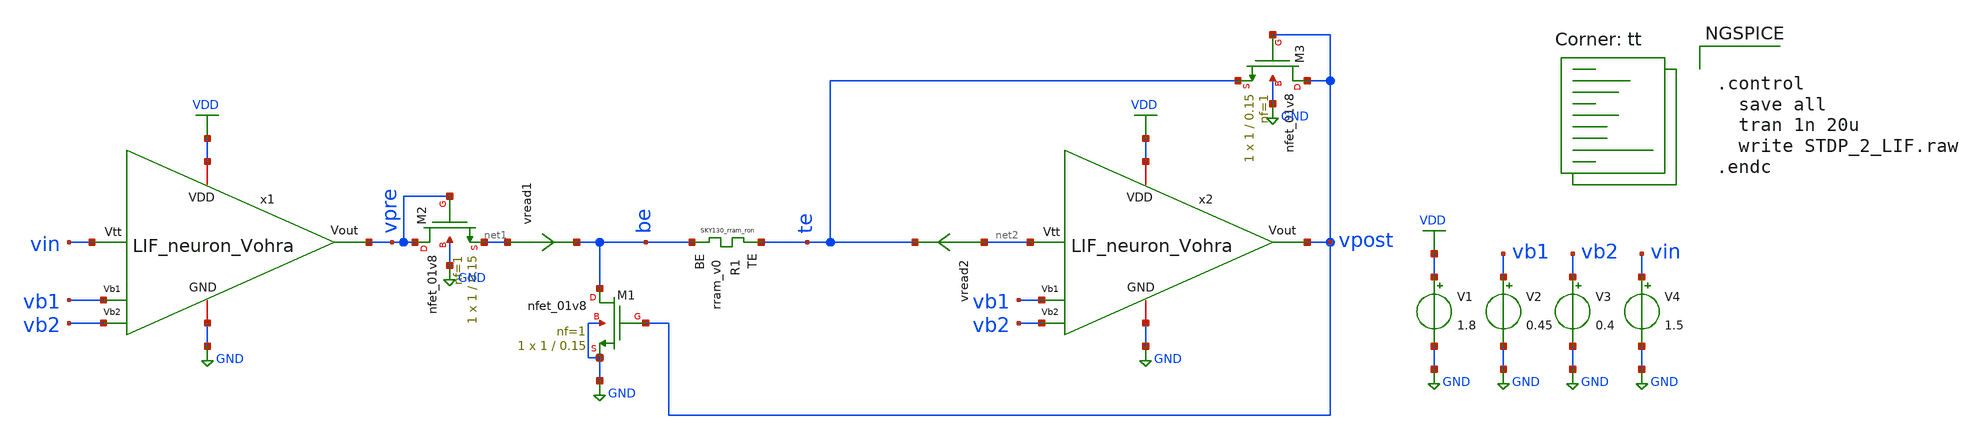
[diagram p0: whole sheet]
** sch_path: STDP/STDP_2_LIF.sch
**.subckt STDP_2_LIF
x1 VDD vpre vb1 vin GND vb2 LIF_neuron_Vohra
XR1 te be rram_v0
x2 VDD vpost vb1 net2 GND vb2 LIF_neuron_Vohra
vread1 net1 be 0
.save i(vread1)
XM1 be vpost GND GND sky130_fd_pr__nfet_01v8 L=0.15 W=1 nf=1 ad='int((nf+1)/2) * W/nf * 0.29' as='int((nf+2)/2) * W/nf * 0.29'
+ pd='2*int((nf+1)/2) * (W/nf + 0.29)' ps='2*int((nf+2)/2) * (W/nf + 0.29)' nrd='0.29 / W' nrs='0.29 / W'
+ sa=0 sb=0 sd=0 mult=1 m=1
V1 VDD GND 1.8
V4 vin GND 1.5
V2 vb1 GND 0.45
V3 vb2 GND 0.4
vread2 net2 te 0
.save i(vread2)
XM2 vpre vpre net1 GND sky130_fd_pr__nfet_01v8 L=0.15 W=1 nf=1 ad='int((nf+1)/2) * W/nf * 0.29' as='int((nf+2)/2) * W/nf * 0.29'
+ pd='2*int((nf+1)/2) * (W/nf + 0.29)' ps='2*int((nf+2)/2) * (W/nf + 0.29)' nrd='0.29 / W' nrs='0.29 / W'
+ sa=0 sb=0 sd=0 mult=1 m=1
XM3 vpost vpost te GND sky130_fd_pr__nfet_01v8 L=0.15 W=1 nf=1 ad='int((nf+1)/2) * W/nf * 0.29' as='int((nf+2)/2) * W/nf * 0.29'
+ pd='2*int((nf+1)/2) * (W/nf + 0.29)' ps='2*int((nf+2)/2) * (W/nf + 0.29)' nrd='0.29 / W' nrs='0.29 / W'
+ sa=0 sb=0 sd=0 mult=1 m=1
**** begin user architecture code
.lib $::SKYWATER_MODELS/sky130.lib.spice tt

** opencircuitdesign pdks install
.inc $::SKYWATER_MODELS/rram_v0.spice



.control
  save all
  tran 1n 20u
  write STDP_2_LIF.raw
.endc


**** end user architecture code
**.ends

* expanding   symbol:  /home/ricardo/RATT_repos/Proyectos_xschem/LIF_neuron/LIF_neuron_Vohra.sym #
*+ of pins=6
** sym_path: LIF_neuron/LIF_neuron_Vohra.sym
** sch_path: LIF_neuron/LIF_neuron_Vohra.sch
.subckt LIF_neuron_Vohra VDD Vout Vb1 Vtt GND Vb2
*.ipin Vtt
*.iopin GND
*.ipin Vb1
*.ipin Vb2
*.iopin VDD
*.opin Vout
XM1 net4 Vtt GND GND sky130_fd_pr__nfet_01v8 L=1 W=0.6 nf=1 ad='int((nf+1)/2) * W/nf * 0.29' as='int((nf+2)/2) * W/nf * 0.29'
+ pd='2*int((nf+1)/2) * (W/nf + 0.29)' ps='2*int((nf+2)/2) * (W/nf + 0.29)' nrd='0.29 / W' nrs='0.29 / W'
+ sa=0 sb=0 sd=0 mult=1 m=1
XM3 net4 net4 VDD VDD sky130_fd_pr__pfet_01v8 L=1 W=0.6 nf=1 ad='int((nf+1)/2) * W/nf * 0.29' as='int((nf+2)/2) * W/nf * 0.29'
+ pd='2*int((nf+1)/2) * (W/nf + 0.29)' ps='2*int((nf+2)/2) * (W/nf + 0.29)' nrd='0.29 / W' nrs='0.29 / W'
+ sa=0 sb=0 sd=0 mult=1 m=1
XM13 net3 Vb1 GND GND sky130_fd_pr__nfet_01v8 L=0.5 W=5 nf=1 ad='int((nf+1)/2) * W/nf * 0.29' as='int((nf+2)/2) * W/nf * 0.29'
+ pd='2*int((nf+1)/2) * (W/nf + 0.29)' ps='2*int((nf+2)/2) * (W/nf + 0.29)' nrd='0.29 / W' nrs='0.29 / W'
+ sa=0 sb=0 sd=0 mult=1 m=1
XM12 net1 net2 net3 GND sky130_fd_pr__nfet_01v8 L=1 W=1 nf=1 ad='int((nf+1)/2) * W/nf * 0.29' as='int((nf+2)/2) * W/nf * 0.29'
+ pd='2*int((nf+1)/2) * (W/nf + 0.29)' ps='2*int((nf+2)/2) * (W/nf + 0.29)' nrd='0.29 / W' nrs='0.29 / W'
+ sa=0 sb=0 sd=0 mult=1 m=1
XM11 net1 net2 VDD VDD sky130_fd_pr__pfet_01v8 L=1 W=1 nf=1 ad='int((nf+1)/2) * W/nf * 0.29' as='int((nf+2)/2) * W/nf * 0.29'
+ pd='2*int((nf+1)/2) * (W/nf + 0.29)' ps='2*int((nf+2)/2) * (W/nf + 0.29)' nrd='0.29 / W' nrs='0.29 / W'
+ sa=0 sb=0 sd=0 mult=1 m=1
XC1 net1 GND sky130_fd_pr__cap_mim_m3_1 W=21 L=1 MF=1 m=1
XM14 net5 net1 GND GND sky130_fd_pr__nfet_01v8 L=1 W=1 nf=1 ad='int((nf+1)/2) * W/nf * 0.29' as='int((nf+2)/2) * W/nf * 0.29'
+ pd='2*int((nf+1)/2) * (W/nf + 0.29)' ps='2*int((nf+2)/2) * (W/nf + 0.29)' nrd='0.29 / W' nrs='0.29 / W'
+ sa=0 sb=0 sd=0 mult=1 m=1
XM4 net5 net4 VDD VDD sky130_fd_pr__pfet_01v8 L=1 W=1 nf=1 ad='int((nf+1)/2) * W/nf * 0.29' as='int((nf+2)/2) * W/nf * 0.29'
+ pd='2*int((nf+1)/2) * (W/nf + 0.29)' ps='2*int((nf+2)/2) * (W/nf + 0.29)' nrd='0.29 / W' nrs='0.29 / W'
+ sa=0 sb=0 sd=0 mult=1 m=1
XC2 net5 GND sky130_fd_pr__cap_mim_m3_1 W=10 L=1 MF=50 m=50
XM5 net5 Vb2 GND GND sky130_fd_pr__nfet_01v8 L=1 W=2 nf=1 ad='int((nf+1)/2) * W/nf * 0.29' as='int((nf+2)/2) * W/nf * 0.29'
+ pd='2*int((nf+1)/2) * (W/nf + 0.29)' ps='2*int((nf+2)/2) * (W/nf + 0.29)' nrd='0.29 / W' nrs='0.29 / W'
+ sa=0 sb=0 sd=0 mult=1 m=1
XM6 net6 Vout GND GND sky130_fd_pr__nfet_01v8 L=1 W=1 nf=1 ad='int((nf+1)/2) * W/nf * 0.29' as='int((nf+2)/2) * W/nf * 0.29'
+ pd='2*int((nf+1)/2) * (W/nf + 0.29)' ps='2*int((nf+2)/2) * (W/nf + 0.29)' nrd='0.29 / W' nrs='0.29 / W'
+ sa=0 sb=0 sd=0 mult=1 m=1
XM7 net2 net5 net6 GND sky130_fd_pr__nfet_01v8 L=1 W=1 nf=1 ad='int((nf+1)/2) * W/nf * 0.29' as='int((nf+2)/2) * W/nf * 0.29'
+ pd='2*int((nf+1)/2) * (W/nf + 0.29)' ps='2*int((nf+2)/2) * (W/nf + 0.29)' nrd='0.29 / W' nrs='0.29 / W'
+ sa=0 sb=0 sd=0 mult=1 m=1
XM8 net2 net5 VDD VDD sky130_fd_pr__pfet_01v8 L=1 W=1 nf=1 ad='int((nf+1)/2) * W/nf * 0.29' as='int((nf+2)/2) * W/nf * 0.29'
+ pd='2*int((nf+1)/2) * (W/nf + 0.29)' ps='2*int((nf+2)/2) * (W/nf + 0.29)' nrd='0.29 / W' nrs='0.29 / W'
+ sa=0 sb=0 sd=0 mult=1 m=1
XM9 Vout net2 net6 GND sky130_fd_pr__nfet_01v8 L=1 W=1 nf=1 ad='int((nf+1)/2) * W/nf * 0.29' as='int((nf+2)/2) * W/nf * 0.29'
+ pd='2*int((nf+1)/2) * (W/nf + 0.29)' ps='2*int((nf+2)/2) * (W/nf + 0.29)' nrd='0.29 / W' nrs='0.29 / W'
+ sa=0 sb=0 sd=0 mult=1 m=1
XM10 Vout net2 VDD VDD sky130_fd_pr__pfet_01v8 L=1 W=5 nf=1 ad='int((nf+1)/2) * W/nf * 0.29' as='int((nf+2)/2) * W/nf * 0.29'
+ pd='2*int((nf+1)/2) * (W/nf + 0.29)' ps='2*int((nf+2)/2) * (W/nf + 0.29)' nrd='0.29 / W' nrs='0.29 / W'
+ sa=0 sb=0 sd=0 mult=1 m=1
.ends

.GLOBAL VDD
.GLOBAL GND
.end
